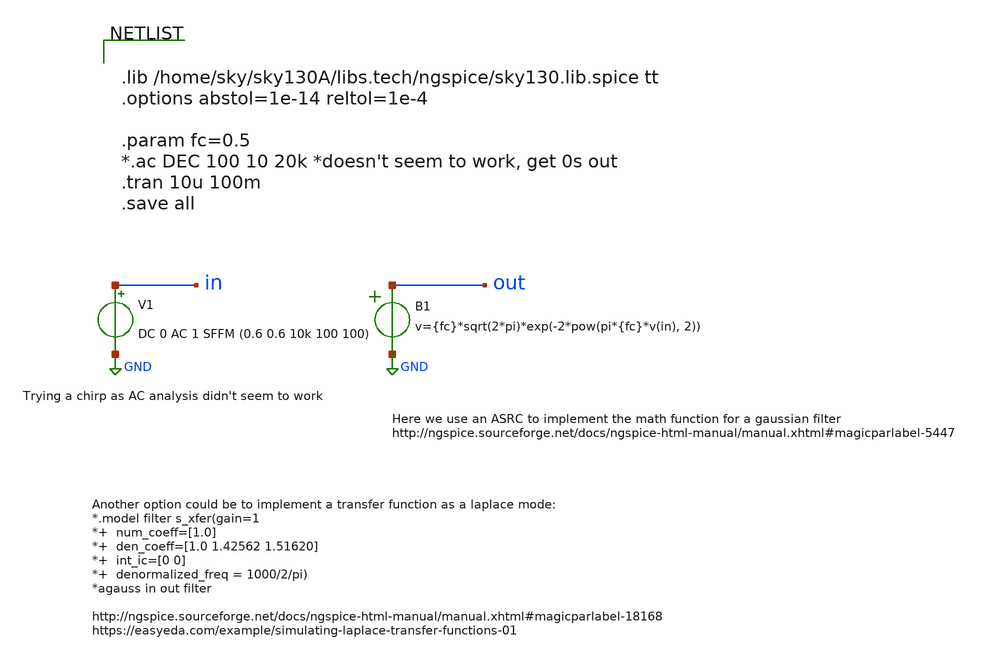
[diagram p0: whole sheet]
** sch_path: xschem/Switched_Caps/asrc_ideal_gaussian_tb.sch
**.subckt asrc_ideal_gaussian_tb
V1 in GND DC 0 AC 1 SFFM (0.6 0.6 10k 100 100)
B1 out GND v={fc}*sqrt(2*pi)*exp(-2*pow(pi*{fc}*v(in), 2))
**** begin user architecture code


.lib /home/sky/sky130A/libs.tech/ngspice/sky130.lib.spice tt
.options abstol=1e-14 reltol=1e-4

.param fc=0.5
*.ac DEC 100 10 20k *doesn't seem to work, get 0s out
.tran 10u 100m
.save all


**** end user architecture code
**.ends
.GLOBAL GND
.end
